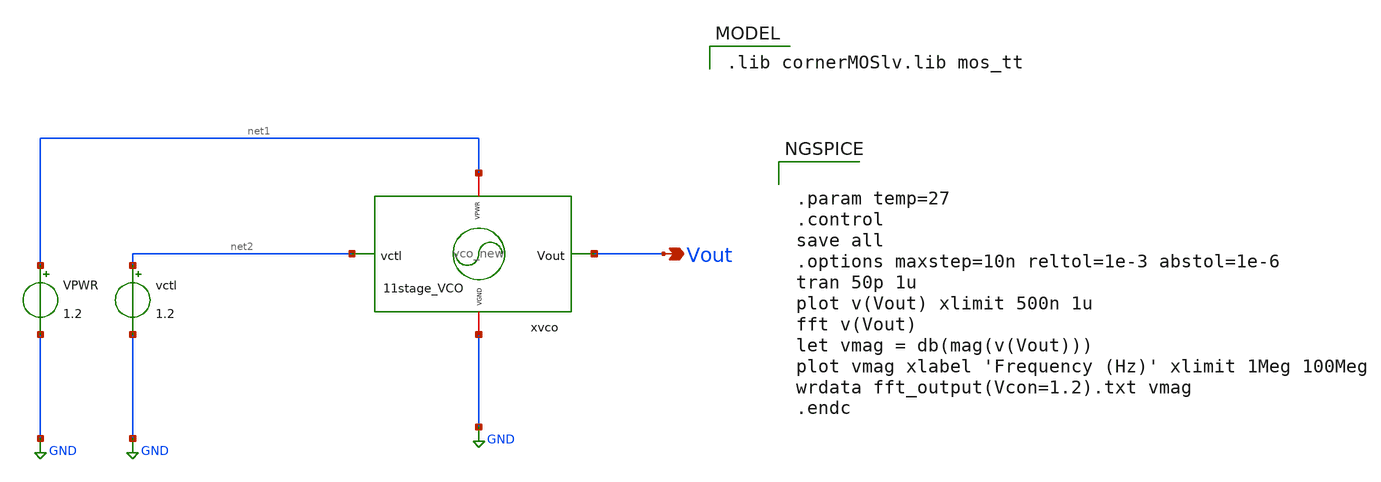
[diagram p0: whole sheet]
** sch_path: Combined Design/design_data/xschem/vco_new_tb.sch
**.subckt vco_new_tb Vout
*.opin Vout
VPWR net1 GND 1.2
vctl net2 GND 1.2
x1 net1 GND net2 Vout vco_new
**** begin user architecture code
 .lib cornerMOSlv.lib mos_tt



.param temp=27
.control
save all
.options maxstep=10n reltol=1e-3 abstol=1e-6
tran 50p 1u
plot v(Vout) xlimit 500n 1u
fft v(Vout)
let vmag = db(mag(v(Vout)))
plot vmag xlabel 'Frequency (Hz)' xlimit 1Meg 100Meg
wrdata fft_output(Vcon=1.2).txt vmag
.endc


**** end user architecture code
**.ends
.GLOBAL GND
.end
